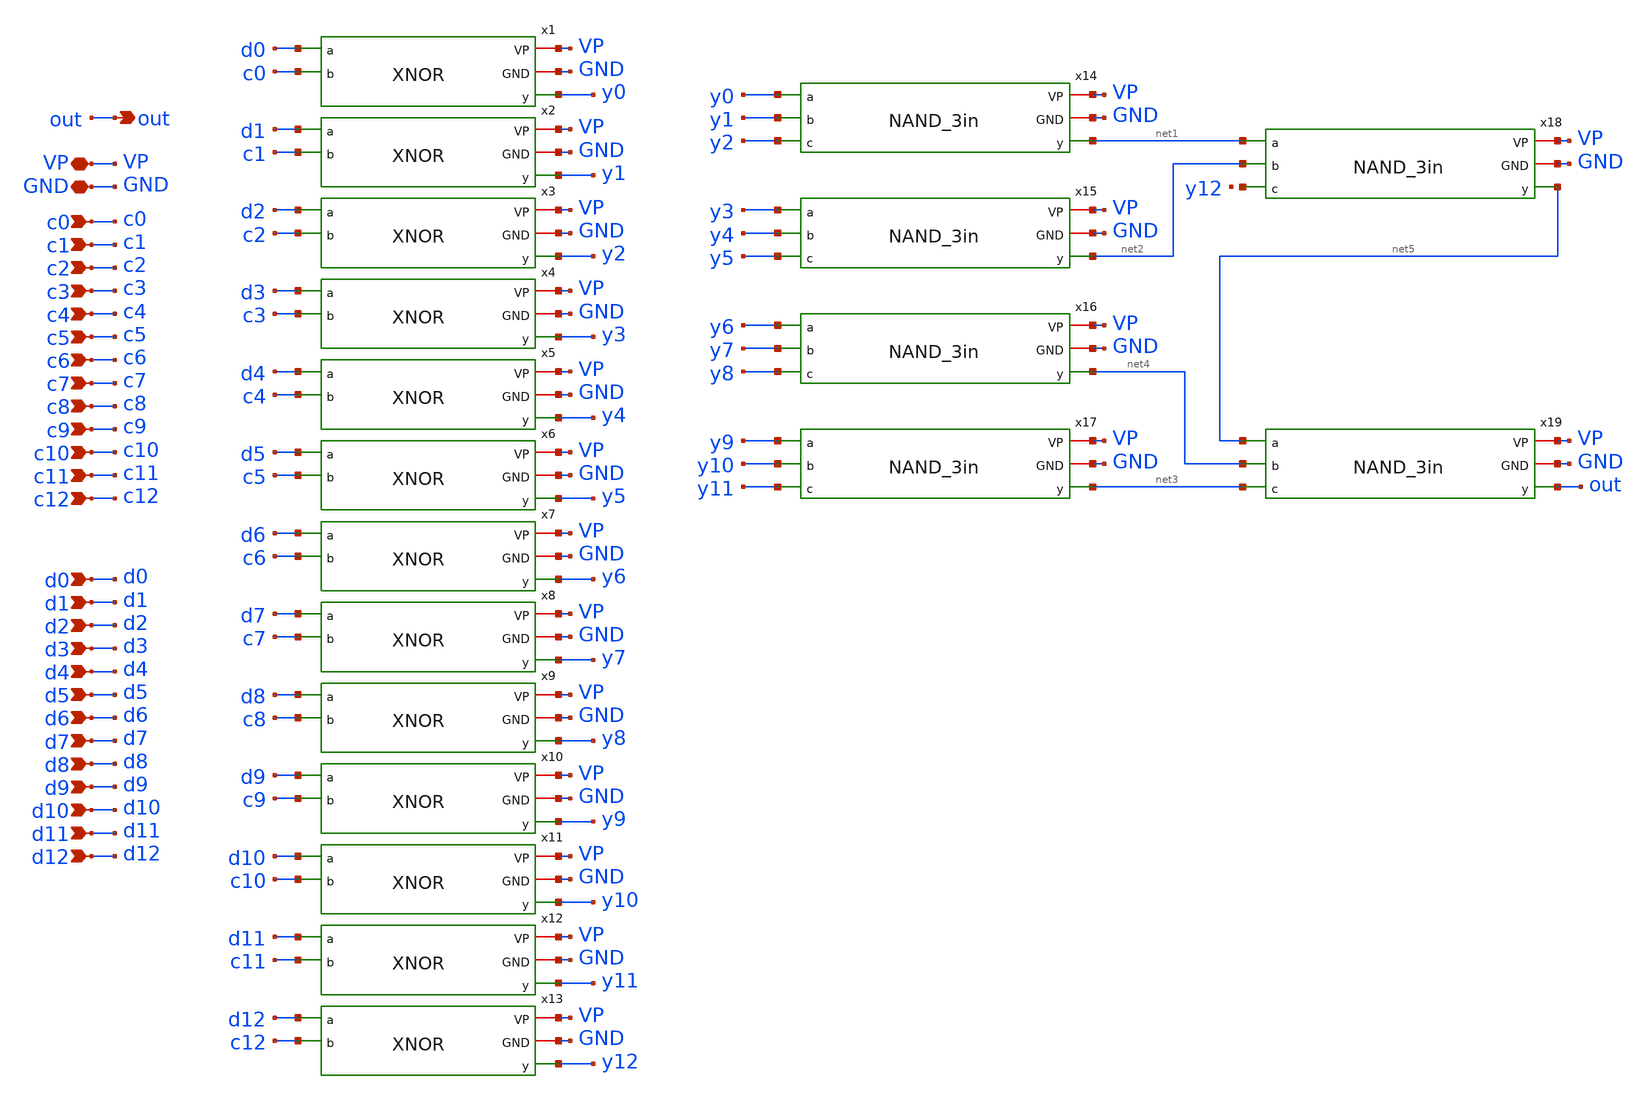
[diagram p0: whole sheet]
** sch_path: divider/schematics/count_data_check.sch
**.subckt count_data_check GND c0 VP c1 out c2 c3 c4 c5 c6 c7 c8 c9 c10 c11 c12 d0 d1 d3 d4 d5 d6 d7
*+ d8 d9 d10 d11 d12 d2
*.iopin GND
*.ipin c0
*.iopin VP
*.ipin c1
*.opin out
*.ipin c2
*.ipin c3
*.ipin c4
*.ipin c5
*.ipin c6
*.ipin c7
*.ipin c8
*.ipin c9
*.ipin c10
*.ipin c11
*.ipin c12
*.ipin d0
*.ipin d1
*.ipin d3
*.ipin d4
*.ipin d5
*.ipin d6
*.ipin d7
*.ipin d8
*.ipin d9
*.ipin d10
*.ipin d11
*.ipin d12
*.ipin d2
x1 VP GND d0 y0 c0 XNOR
x2 VP GND d1 y1 c1 XNOR
x3 VP GND d2 y2 c2 XNOR
x4 VP GND d3 y3 c3 XNOR
x5 VP GND d4 y4 c4 XNOR
x6 VP GND d5 y5 c5 XNOR
x7 VP GND d6 y6 c6 XNOR
x8 VP GND d7 y7 c7 XNOR
x9 VP GND d8 y8 c8 XNOR
x10 VP GND d9 y9 c9 XNOR
x11 VP GND d10 y10 c10 XNOR
x12 VP GND d11 y11 c11 XNOR
x13 VP GND d12 y12 c12 XNOR
x14 VP GND y0 net1 y1 y2 NAND_3in
x15 VP GND y3 net2 y4 y5 NAND_3in
x16 VP GND y6 net4 y7 y8 NAND_3in
x17 VP GND y9 net3 y10 y11 NAND_3in
x18 VP GND net1 net5 net2 net6 NAND_3in
x19 VP GND net5 out net4 net3 NAND_3in
**.ends
.end
